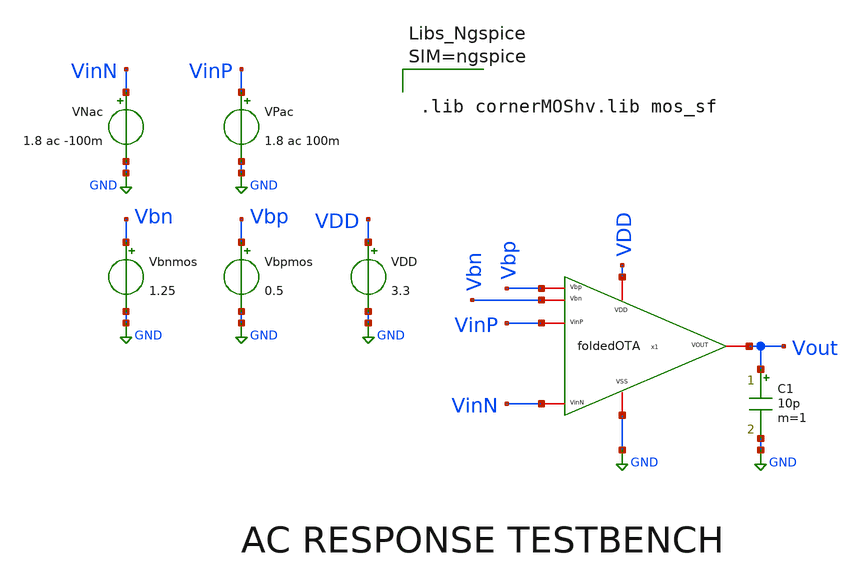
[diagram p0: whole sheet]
** sch_path: ac/AC-foldedOTA.sch
* v1_ideal_current_sources/schematic/foldedOTA.sch:
* (c) 2026 Fares Satouh
**.subckt AC-foldedOTA
VPac VinP GND 1.8 ac 100m
VNac VinN GND 1.8 ac -100m
Vbnmos Vbn GND 1.25
Vbpmos Vbp GND 0.5
VDD VDD GND 3.3
x1 VDD Vbp Vout VinP VinN Vbn GND foldedOTA
C1 Vout GND 10p m=1
**** begin user architecture code



.lib cornerMOShv.lib mos_sf





.control
destroy all

ac dec 20 1 100Meg
run

let VinDiff = v(VinP) - v(VinN)
let gain_db = db(Vout/VinDiff)
let gain_phase = phase(Vout/VinDiff)*180/PI

save all

meas ac dc_gain      find gain_db at=1
meas ac f3db         when gain_db='dc_gain-3'
meas ac gbw          when gain_db=0
meas ac phase_at_gbw find gain_phase when gain_db=0
let phase_margin = 180 + phase_at_gbw

plot gain_db
plot gain_phase
plot gain_db gain_phase

print dc_gain
print f3db
print gbw
print phase_margin
.endc


**** end user architecture code
**.ends

* expanding   symbol:  foldedOTA.sym # of pins=7
** sym_path: v1_ideal_current_sources/schematic/foldedOTA.sym
** sch_path: v1_ideal_current_sources/schematic/foldedOTA.sch
.subckt foldedOTA VDD Vbp VOUT VinP VinN Vbn VSS
*.iopin VDD
*.iopin VSS
*.iopin VOUT
*.iopin Vbp
*.iopin Vbn
*.iopin VinN
*.iopin VinP
XM1 net2 VinP net1 VSS sg13_hv_nmos w=28u l=1u ng=4 m=1 mm_ok=1
XM2 net3 VinN net1 VSS sg13_hv_nmos w=28u l=1u ng=4 m=1 mm_ok=1
XM3 net1 net8 VSS VSS sg13_hv_nmos w=15u l=1u ng=3 m=1 mm_ok=1
XM4 net2 net7 VDD VDD sg13_hv_pmos w=14u l=1u ng=2 m=1 mm_ok=1
XM5 net3 net7 VDD VDD sg13_hv_pmos w=14u l=1u ng=2 m=1 mm_ok=1
XM6 net4 Vbp net2 VDD sg13_hv_pmos w=2u l=1u ng=1 m=1 mm_ok=1
XM7 VOUT Vbp net3 VDD sg13_hv_pmos w=2u l=1u ng=1 m=1 mm_ok=1
XM8 net4 Vbn net5 VSS sg13_hv_nmos w=7u l=1u ng=1 m=1 mm_ok=1
XM9 VOUT Vbn net6 VSS sg13_hv_nmos w=7u l=1u ng=1 m=1 mm_ok=1
XM10 net5 net4 VSS VSS sg13_hv_nmos w=7u l=1u ng=1 m=1 mm_ok=1
XM11 net6 net4 VSS VSS sg13_hv_nmos w=7u l=1u ng=1 m=1 mm_ok=1
XM12 net8 net8 VSS VSS sg13_hv_nmos w=15u l=1u ng=3 m=1 mm_ok=1
I0 VDD net8 50u
XM13 net7 net7 VDD VDD sg13_hv_pmos w=14u l=1u ng=2 m=1 mm_ok=1
I1 net7 VSS 50u
.ends

.GLOBAL GND
.end
